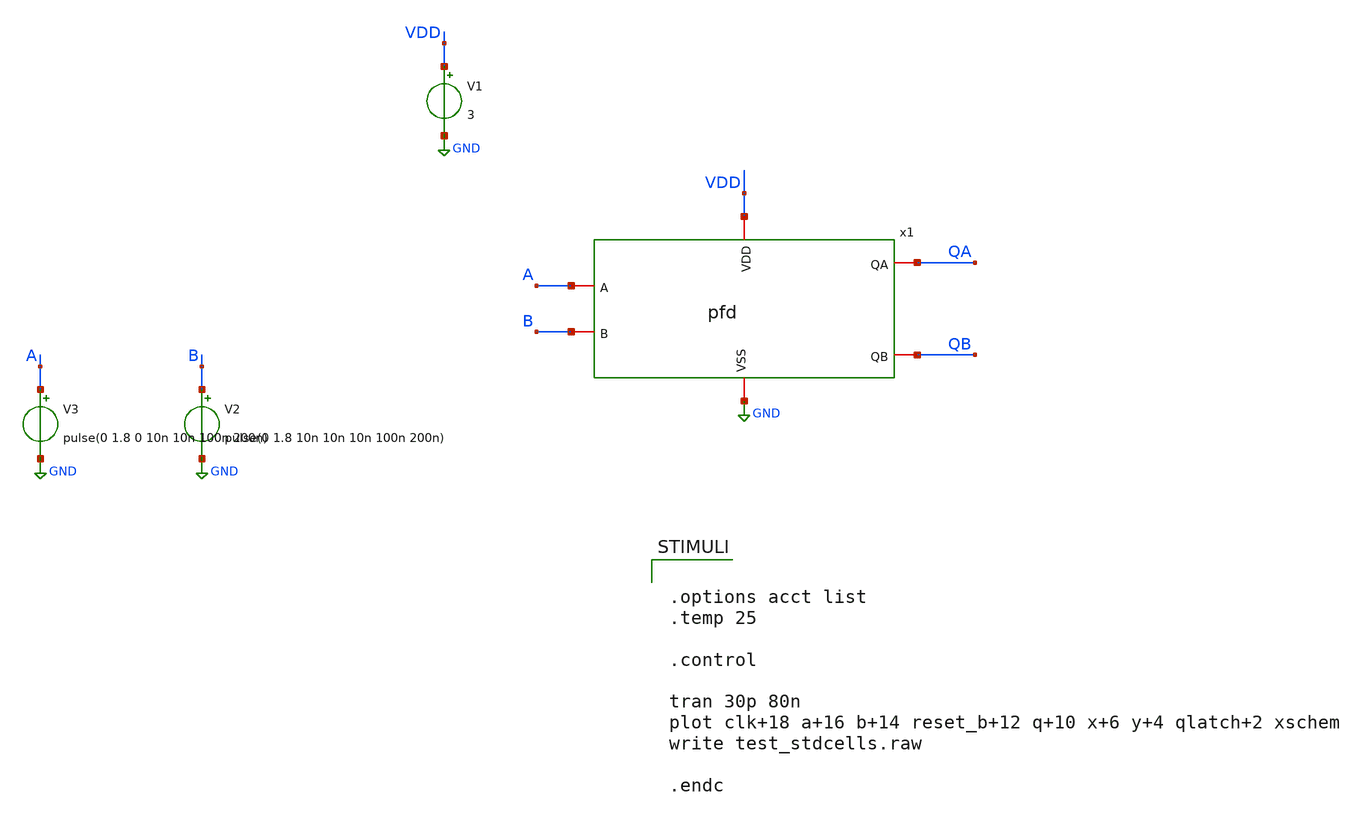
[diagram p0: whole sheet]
** sch_path: xschem01/pfd/untitled-1.sch
**.subckt untitled-1
x1 GND VDD A QA QB B pfd
V1 VDD GND 3
V2 B GND pulse(0 1.8 10n 10n 10n 100n 200n)
V3 A GND pulse(0 1.8 0 10n 10n 100n 200n)
**** begin user architecture code

** opencircuitdesign pdks install
.lib $::SKYWATER_MODELS/sky130.lib.spice tt




.options acct list
.temp 25

.control

tran 30p 80n
plot clk+18 a+16 b+14 reset_b+12 q+10 x+6 y+4 qlatch+2 xschem
write test_stdcells.raw

.endc


**** end user architecture code
**.ends
.GLOBAL GND
.end
